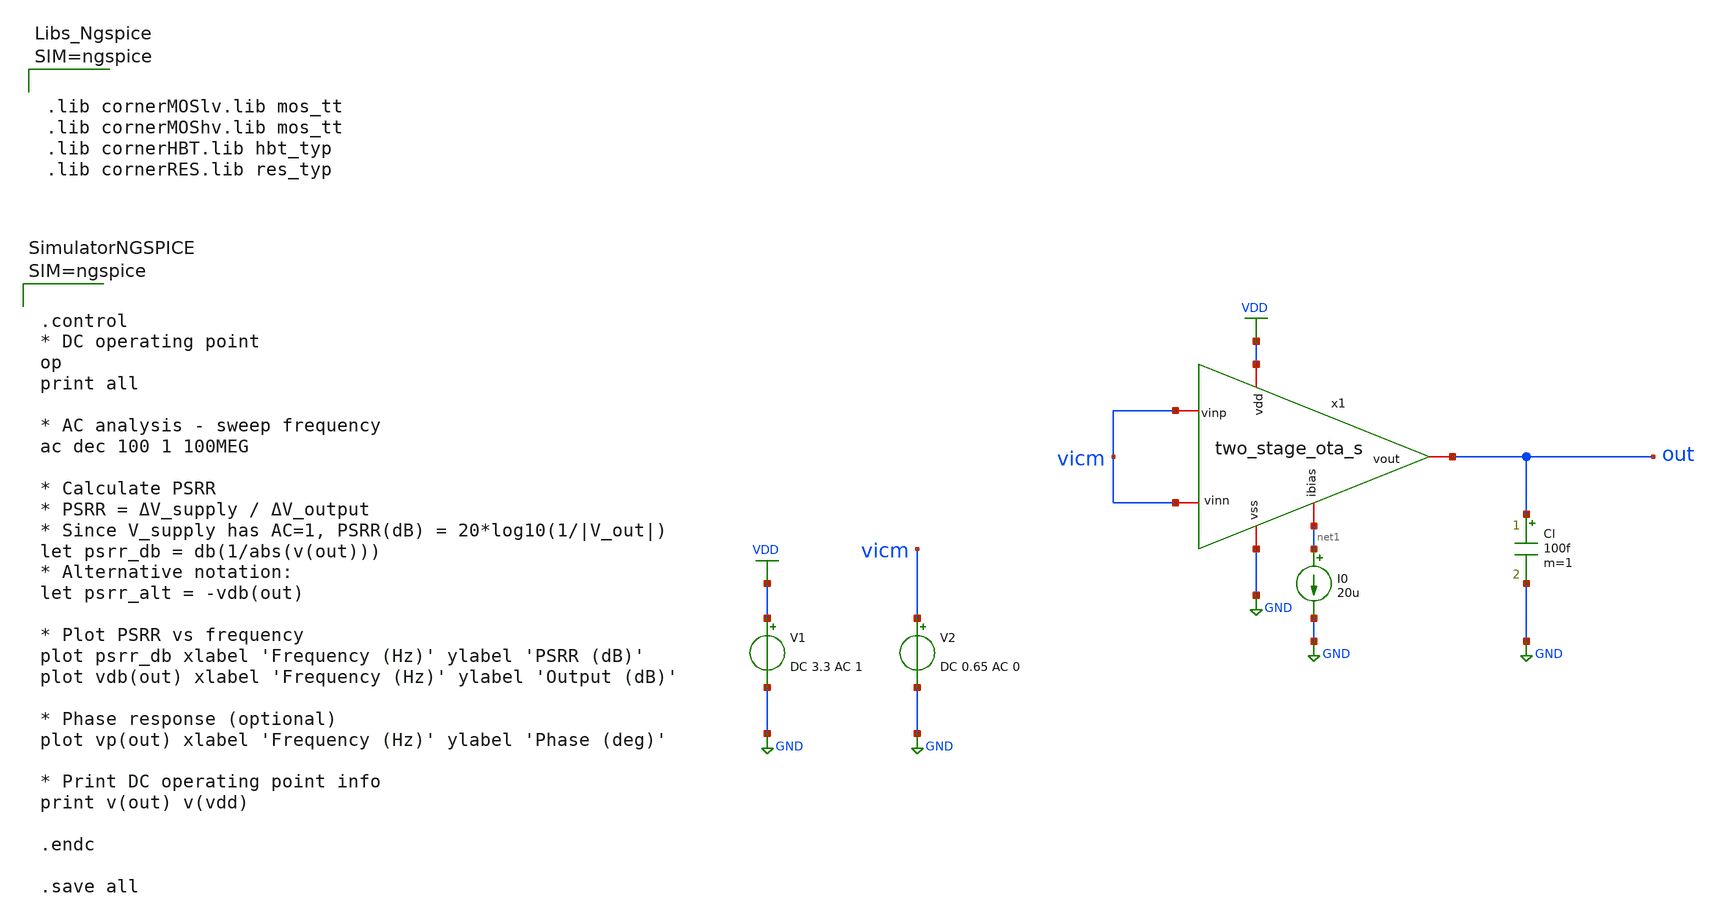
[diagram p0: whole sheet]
** sch_path: dependencies/pmu_ip/dependencies/OTA/OTA-main/testbenches/two_stage_ota_s_psrr.sch
**.subckt two_stage_ota_s_psrr
I0 net1 GND 20u
Cl out GND 100f m=1
x1 VDD net1 vicm vicm out GND two_stage_ota_s
V1 VDD GND DC 3.3 AC 1
V2 vicm GND DC 0.65 AC 0
**** begin user architecture code



.control
* DC operating point
op
print all

* AC analysis - sweep frequency
ac dec 100 1 100MEG

* Calculate PSRR
* PSRR = ΔV_supply / ΔV_output
* Since V_supply has AC=1, PSRR(dB) = 20*log10(1/|V_out|)
let psrr_db = db(1/abs(v(out)))
* Alternative notation:
let psrr_alt = -vdb(out)

* Plot PSRR vs frequency
plot psrr_db xlabel 'Frequency (Hz)' ylabel 'PSRR (dB)'
plot vdb(out) xlabel 'Frequency (Hz)' ylabel 'Output (dB)'

* Phase response (optional)
plot vp(out) xlabel 'Frequency (Hz)' ylabel 'Phase (deg)'

* Print DC operating point info
print v(out) v(vdd)

.endc

.save all






.lib cornerMOSlv.lib mos_tt
.lib cornerMOShv.lib mos_tt
.lib cornerHBT.lib hbt_typ
.lib cornerRES.lib res_typ



**** end user architecture code
**.ends

* expanding   symbol:  /foss/designs/bandgap_refrence_ihp/two_stage_ota/two_stage_ota_s.sym # of
*+ pins=6
** sym_path: dependencies/pmu_ip/dependencies/OTA/OTA-main/testbenches/two_stage_ota_s.sym
** sch_path: dependencies/pmu_ip/dependencies/OTA/OTA-main/testbenches/two_stage_ota_s.sch
.subckt two_stage_ota_s vdd ibias vinn vinp vout vss
*.iopin ibias
*.iopin vdd
*.iopin vss
*.iopin vout
*.iopin vinp
*.iopin vinn
C1 net4 vout 350f m=1
R1 net3 net4 4k m=1
XM4 net3 net2 vss vss sg13_hv_nmos w=3u l=1u ng=1 m=1 mm_ok=1
XM3 net2 net2 vss vss sg13_hv_nmos w=3u l=1u ng=1 m=1 mm_ok=1
XM1 net3 vinp net1 vdd sg13_hv_pmos w=12u l=1u ng=1 m=2 mm_ok=1
XM2 net2 vinn net1 vdd sg13_hv_pmos w=12u l=1u ng=1 m=2 mm_ok=1
XM5 net1 ibias vdd vdd sg13_hv_pmos w=6u l=3u ng=1 m=2 mm_ok=1
XM7 vout ibias vdd vdd sg13_hv_pmos w=6u l=3u ng=1 m=8 mm_ok=1
XM8 ibias ibias vdd vdd sg13_hv_pmos w=6u l=3u ng=1 m=8 mm_ok=1
XM9 vout net3 vss vss sg13_hv_nmos w=12u l=1u ng=1 m=2 mm_ok=1
.ends

.GLOBAL GND
.GLOBAL VDD
.end
